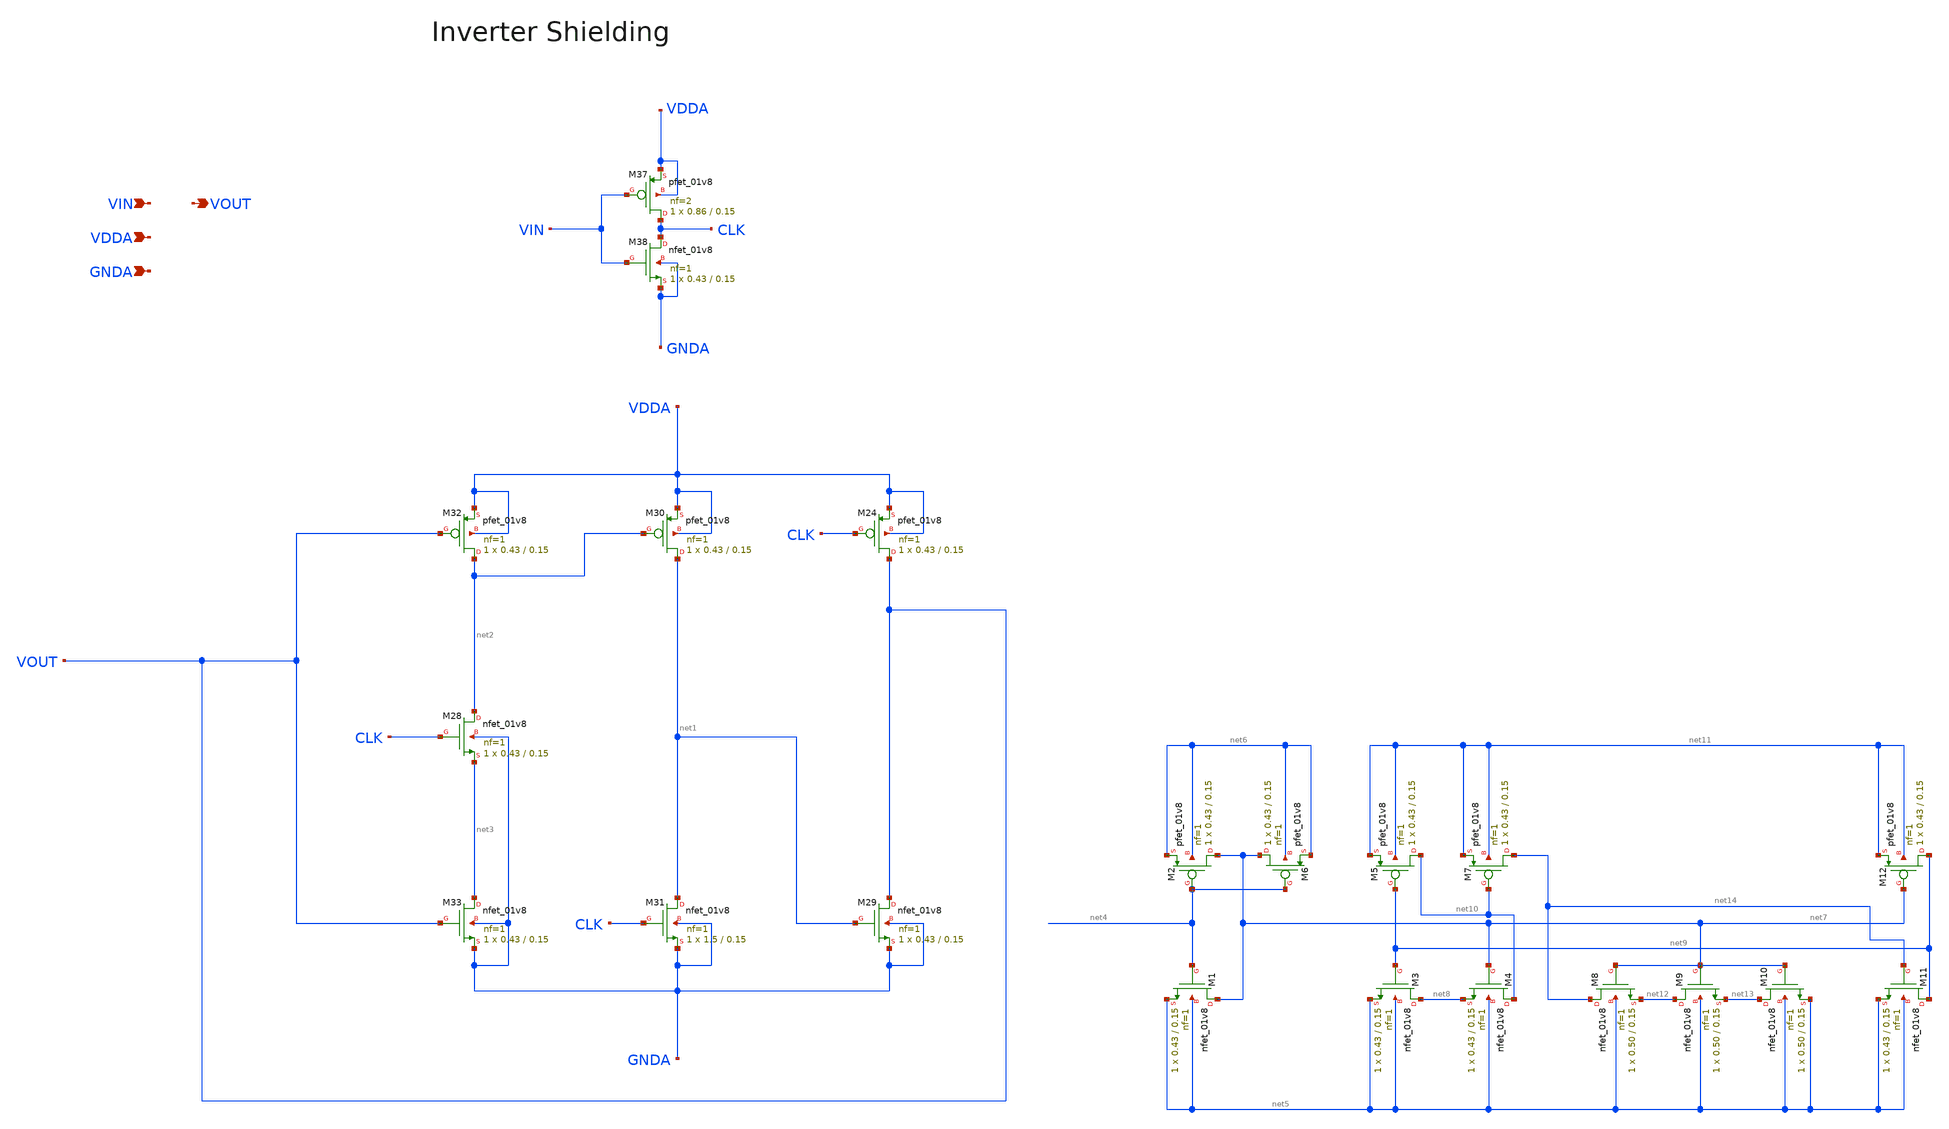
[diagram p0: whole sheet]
** sch_path: projects/pll/divider/xschem_ngspice/TSPC_FF_ratioed_divide2_3.sch
**.subckt TSPC_FF_ratioed_divide2_3 VIN VOUT VDDA GNDA
*.ipin VIN
*.opin VOUT
*.ipin VDDA
*.ipin GNDA
XM24 VOUT CLK VDDA VDDA sky130_fd_pr__pfet_01v8 L=0.15 W=0.43 nf=1 ad='int((nf+1)/2) * W/nf * 0.29' as='int((nf+2)/2) * W/nf * 0.29'
+ pd='2*int((nf+1)/2) * (W/nf + 0.29)' ps='2*int((nf+2)/2) * (W/nf + 0.29)' nrd='0.29 / W' nrs='0.29 / W'
+ sa=0 sb=0 sd=0 mult=1 m=1
XM29 VOUT net1 GNDA GNDA sky130_fd_pr__nfet_01v8 L=0.15 W=0.43 nf=1 ad='int((nf+1)/2) * W/nf * 0.29'
+ as='int((nf+2)/2) * W/nf * 0.29' pd='2*int((nf+1)/2) * (W/nf + 0.29)' ps='2*int((nf+2)/2) * (W/nf + 0.29)'
+ nrd='0.29 / W' nrs='0.29 / W' sa=0 sb=0 sd=0 mult=1 m=1
XM30 net1 net2 VDDA VDDA sky130_fd_pr__pfet_01v8 L=0.15 W=0.43 nf=1 ad='int((nf+1)/2) * W/nf * 0.29'
+ as='int((nf+2)/2) * W/nf * 0.29' pd='2*int((nf+1)/2) * (W/nf + 0.29)' ps='2*int((nf+2)/2) * (W/nf + 0.29)'
+ nrd='0.29 / W' nrs='0.29 / W' sa=0 sb=0 sd=0 mult=1 m=1
XM31 net1 CLK GNDA GNDA sky130_fd_pr__nfet_01v8 L=0.15 W=1.5 nf=1 ad='int((nf+1)/2) * W/nf * 0.29' as='int((nf+2)/2) * W/nf * 0.29'
+ pd='2*int((nf+1)/2) * (W/nf + 0.29)' ps='2*int((nf+2)/2) * (W/nf + 0.29)' nrd='0.29 / W' nrs='0.29 / W'
+ sa=0 sb=0 sd=0 mult=1 m=1
XM32 net2 VOUT VDDA VDDA sky130_fd_pr__pfet_01v8 L=0.15 W=0.43 nf=1 ad='int((nf+1)/2) * W/nf * 0.29'
+ as='int((nf+2)/2) * W/nf * 0.29' pd='2*int((nf+1)/2) * (W/nf + 0.29)' ps='2*int((nf+2)/2) * (W/nf + 0.29)'
+ nrd='0.29 / W' nrs='0.29 / W' sa=0 sb=0 sd=0 mult=1 m=1
XM33 net3 VOUT GNDA GNDA sky130_fd_pr__nfet_01v8 L=0.15 W=0.43 nf=1 ad='int((nf+1)/2) * W/nf * 0.29'
+ as='int((nf+2)/2) * W/nf * 0.29' pd='2*int((nf+1)/2) * (W/nf + 0.29)' ps='2*int((nf+2)/2) * (W/nf + 0.29)'
+ nrd='0.29 / W' nrs='0.29 / W' sa=0 sb=0 sd=0 mult=1 m=1
XM28 net2 CLK net3 GNDA sky130_fd_pr__nfet_01v8 L=0.15 W=0.43 nf=1 ad='int((nf+1)/2) * W/nf * 0.29' as='int((nf+2)/2) * W/nf * 0.29'
+ pd='2*int((nf+1)/2) * (W/nf + 0.29)' ps='2*int((nf+2)/2) * (W/nf + 0.29)' nrd='0.29 / W' nrs='0.29 / W'
+ sa=0 sb=0 sd=0 mult=1 m=1
XM37 CLK VIN VDDA VDDA sky130_fd_pr__pfet_01v8 L=0.15 W=0.86 nf=2 ad='int((nf+1)/2) * W/nf * 0.29' as='int((nf+2)/2) * W/nf * 0.29'
+ pd='2*int((nf+1)/2) * (W/nf + 0.29)' ps='2*int((nf+2)/2) * (W/nf + 0.29)' nrd='0.29 / W' nrs='0.29 / W'
+ sa=0 sb=0 sd=0 mult=1 m=1
XM38 CLK VIN GNDA GNDA sky130_fd_pr__nfet_01v8 L=0.15 W=0.43 nf=1 ad='int((nf+1)/2) * W/nf * 0.29' as='int((nf+2)/2) * W/nf * 0.29'
+ pd='2*int((nf+1)/2) * (W/nf + 0.29)' ps='2*int((nf+2)/2) * (W/nf + 0.29)' nrd='0.29 / W' nrs='0.29 / W'
+ sa=0 sb=0 sd=0 mult=1 m=1
XM1 net7 net4 net5 net5 sky130_fd_pr__nfet_01v8 L=0.15 W=0.43 nf=1 ad='int((nf+1)/2) * W/nf * 0.29' as='int((nf+2)/2) * W/nf * 0.29'
+ pd='2*int((nf+1)/2) * (W/nf + 0.29)' ps='2*int((nf+2)/2) * (W/nf + 0.29)' nrd='0.29 / W' nrs='0.29 / W'
+ sa=0 sb=0 sd=0 mult=1 m=1
XM2 net7 net4 net6 net6 sky130_fd_pr__pfet_01v8 L=0.15 W=0.43 nf=1 ad='int((nf+1)/2) * W/nf * 0.29' as='int((nf+2)/2) * W/nf * 0.29'
+ pd='2*int((nf+1)/2) * (W/nf + 0.29)' ps='2*int((nf+2)/2) * (W/nf + 0.29)' nrd='0.29 / W' nrs='0.29 / W'
+ sa=0 sb=0 sd=0 mult=1 m=1
XM3 net8 net9 net5 net5 sky130_fd_pr__nfet_01v8 L=0.15 W=0.43 nf=1 ad='int((nf+1)/2) * W/nf * 0.29' as='int((nf+2)/2) * W/nf * 0.29'
+ pd='2*int((nf+1)/2) * (W/nf + 0.29)' ps='2*int((nf+2)/2) * (W/nf + 0.29)' nrd='0.29 / W' nrs='0.29 / W'
+ sa=0 sb=0 sd=0 mult=1 m=1
XM4 net10 net7 net8 net5 sky130_fd_pr__nfet_01v8 L=0.15 W=0.43 nf=1 ad='int((nf+1)/2) * W/nf * 0.29'
+ as='int((nf+2)/2) * W/nf * 0.29' pd='2*int((nf+1)/2) * (W/nf + 0.29)' ps='2*int((nf+2)/2) * (W/nf + 0.29)'
+ nrd='0.29 / W' nrs='0.29 / W' sa=0 sb=0 sd=0 mult=1 m=1
XM5 net10 net9 net11 net11 sky130_fd_pr__pfet_01v8 L=0.15 W=0.43 nf=1 ad='int((nf+1)/2) * W/nf * 0.29'
+ as='int((nf+2)/2) * W/nf * 0.29' pd='2*int((nf+1)/2) * (W/nf + 0.29)' ps='2*int((nf+2)/2) * (W/nf + 0.29)'
+ nrd='0.29 / W' nrs='0.29 / W' sa=0 sb=0 sd=0 mult=1 m=1
XM6 net7 net4 net6 net6 sky130_fd_pr__pfet_01v8 L=0.15 W=0.43 nf=1 ad='int((nf+1)/2) * W/nf * 0.29' as='int((nf+2)/2) * W/nf * 0.29'
+ pd='2*int((nf+1)/2) * (W/nf + 0.29)' ps='2*int((nf+2)/2) * (W/nf + 0.29)' nrd='0.29 / W' nrs='0.29 / W'
+ sa=0 sb=0 sd=0 mult=1 m=1
XM7 net14 net10 net11 net11 sky130_fd_pr__pfet_01v8 L=0.15 W=0.43 nf=1 ad='int((nf+1)/2) * W/nf * 0.29'
+ as='int((nf+2)/2) * W/nf * 0.29' pd='2*int((nf+1)/2) * (W/nf + 0.29)' ps='2*int((nf+2)/2) * (W/nf + 0.29)'
+ nrd='0.29 / W' nrs='0.29 / W' sa=0 sb=0 sd=0 mult=1 m=1
XM8 net14 net7 net12 net5 sky130_fd_pr__nfet_01v8 L=0.15 W=0.50 nf=1 ad='int((nf+1)/2) * W/nf * 0.29'
+ as='int((nf+2)/2) * W/nf * 0.29' pd='2*int((nf+1)/2) * (W/nf + 0.29)' ps='2*int((nf+2)/2) * (W/nf + 0.29)'
+ nrd='0.29 / W' nrs='0.29 / W' sa=0 sb=0 sd=0 mult=1 m=1
XM9 net12 net7 net13 net5 sky130_fd_pr__nfet_01v8 L=0.15 W=0.50 nf=1 ad='int((nf+1)/2) * W/nf * 0.29'
+ as='int((nf+2)/2) * W/nf * 0.29' pd='2*int((nf+1)/2) * (W/nf + 0.29)' ps='2*int((nf+2)/2) * (W/nf + 0.29)'
+ nrd='0.29 / W' nrs='0.29 / W' sa=0 sb=0 sd=0 mult=1 m=1
XM10 net13 net7 net5 net5 sky130_fd_pr__nfet_01v8 L=0.15 W=0.50 nf=1 ad='int((nf+1)/2) * W/nf * 0.29'
+ as='int((nf+2)/2) * W/nf * 0.29' pd='2*int((nf+1)/2) * (W/nf + 0.29)' ps='2*int((nf+2)/2) * (W/nf + 0.29)'
+ nrd='0.29 / W' nrs='0.29 / W' sa=0 sb=0 sd=0 mult=1 m=1
XM11 net9 net14 net5 net5 sky130_fd_pr__nfet_01v8 L=0.15 W=0.43 nf=1 ad='int((nf+1)/2) * W/nf * 0.29'
+ as='int((nf+2)/2) * W/nf * 0.29' pd='2*int((nf+1)/2) * (W/nf + 0.29)' ps='2*int((nf+2)/2) * (W/nf + 0.29)'
+ nrd='0.29 / W' nrs='0.29 / W' sa=0 sb=0 sd=0 mult=1 m=1
XM12 net9 net7 net11 net11 sky130_fd_pr__pfet_01v8 L=0.15 W=0.43 nf=1 ad='int((nf+1)/2) * W/nf * 0.29'
+ as='int((nf+2)/2) * W/nf * 0.29' pd='2*int((nf+1)/2) * (W/nf + 0.29)' ps='2*int((nf+2)/2) * (W/nf + 0.29)'
+ nrd='0.29 / W' nrs='0.29 / W' sa=0 sb=0 sd=0 mult=1 m=1
**.ends
.end
